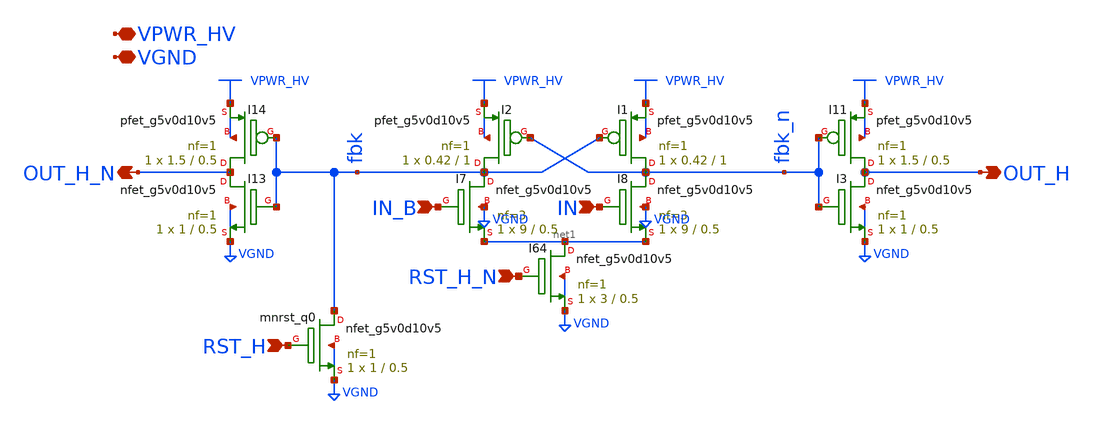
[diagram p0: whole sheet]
** sch_path: gpiov2_amux_ctl_lshv2hv.sch
* Copyright 2023 David Mitchell Bailey
* Licensed under the Apache License, Version 2.0 (the "License");
* you may not use this file except in compliance with the License.
* You may obtain a copy of the License at
* https://www.apache.org/licenses/LICENSE-2.0
* Unless required by applicable law or agreed to in writing, software
* distributed under the License is distributed on an "AS IS" BASIS,
* WITHOUT WARRANTIES OR CONDITIONS OF ANY KIND, either express or implied.
* See the License for the specific language governing permissions and
* limitations under the License.
**.subckt gpiov2_amux_ctl_lshv2hv RST_H OUT_H VPWR_HV VGND OUT_H_N RST_H_N IN_B IN
*.ipin RST_H
*.opin OUT_H
*.iopin VPWR_HV
*.iopin VGND
*.opin OUT_H_N
*.ipin RST_H_N
*.ipin IN_B
*.ipin IN
XI13 OUT_H_N fbk VGND VGND sky130_fd_pr__nfet_g5v0d10v5 L=0.5 W=1 nf=1 ad='int((nf+1)/2) * W/nf * 0.29'
+ as='int((nf+2)/2) * W/nf * 0.29' pd='2*int((nf+1)/2) * (W/nf + 0.29)' ps='2*int((nf+2)/2) * (W/nf + 0.29)'
+ nrd='0.29 / W' nrs='0.29 / W' sa=0 sb=0 sd=0 mult=1 m=1
XI14 OUT_H_N fbk VPWR_HV VPWR_HV sky130_fd_pr__pfet_g5v0d10v5 L=0.5 W=1.5 nf=1 ad='int((nf+1)/2) * W/nf * 0.29'
+ as='int((nf+2)/2) * W/nf * 0.29' pd='2*int((nf+1)/2) * (W/nf + 0.29)' ps='2*int((nf+2)/2) * (W/nf + 0.29)'
+ nrd='0.29 / W' nrs='0.29 / W' sa=0 sb=0 sd=0 mult=1 m=1
XI3 OUT_H fbk_n VGND VGND sky130_fd_pr__nfet_g5v0d10v5 L=0.5 W=1 nf=1 ad='int((nf+1)/2) * W/nf * 0.29'
+ as='int((nf+2)/2) * W/nf * 0.29' pd='2*int((nf+1)/2) * (W/nf + 0.29)' ps='2*int((nf+2)/2) * (W/nf + 0.29)'
+ nrd='0.29 / W' nrs='0.29 / W' sa=0 sb=0 sd=0 mult=1 m=1
XI11 OUT_H fbk_n VPWR_HV VPWR_HV sky130_fd_pr__pfet_g5v0d10v5 L=0.5 W=1.5 nf=1 ad='int((nf+1)/2) * W/nf * 0.29'
+ as='int((nf+2)/2) * W/nf * 0.29' pd='2*int((nf+1)/2) * (W/nf + 0.29)' ps='2*int((nf+2)/2) * (W/nf + 0.29)'
+ nrd='0.29 / W' nrs='0.29 / W' sa=0 sb=0 sd=0 mult=1 m=1
XI8 fbk_n IN net1 VGND sky130_fd_pr__nfet_g5v0d10v5 L=0.5 W=9 nf=3 ad='int((nf+1)/2) * W/nf * 0.29' as='int((nf+2)/2) * W/nf * 0.29'
+ pd='2*int((nf+1)/2) * (W/nf + 0.29)' ps='2*int((nf+2)/2) * (W/nf + 0.29)' nrd='0.29 / W' nrs='0.29 / W'
+ sa=0 sb=0 sd=0 mult=1 m=1
XI1 fbk_n fbk VPWR_HV VPWR_HV sky130_fd_pr__pfet_g5v0d10v5 L=1 W=0.42 nf=1 ad='int((nf+1)/2) * W/nf * 0.29'
+ as='int((nf+2)/2) * W/nf * 0.29' pd='2*int((nf+1)/2) * (W/nf + 0.29)' ps='2*int((nf+2)/2) * (W/nf + 0.29)'
+ nrd='0.29 / W' nrs='0.29 / W' sa=0 sb=0 sd=0 mult=1 m=1
XI7 fbk IN_B net1 VGND sky130_fd_pr__nfet_g5v0d10v5 L=0.5 W=9 nf=3 ad='int((nf+1)/2) * W/nf * 0.29' as='int((nf+2)/2) * W/nf * 0.29'
+ pd='2*int((nf+1)/2) * (W/nf + 0.29)' ps='2*int((nf+2)/2) * (W/nf + 0.29)' nrd='0.29 / W' nrs='0.29 / W'
+ sa=0 sb=0 sd=0 mult=1 m=1
XI2 fbk fbk_n VPWR_HV VPWR_HV sky130_fd_pr__pfet_g5v0d10v5 L=1 W=0.42 nf=1 ad='int((nf+1)/2) * W/nf * 0.29'
+ as='int((nf+2)/2) * W/nf * 0.29' pd='2*int((nf+1)/2) * (W/nf + 0.29)' ps='2*int((nf+2)/2) * (W/nf + 0.29)'
+ nrd='0.29 / W' nrs='0.29 / W' sa=0 sb=0 sd=0 mult=1 m=1
Xmnrst_q0 fbk RST_H VGND VGND sky130_fd_pr__nfet_g5v0d10v5 L=0.5 W=1 nf=1 ad='int((nf+1)/2) * W/nf * 0.29'
+ as='int((nf+2)/2) * W/nf * 0.29' pd='2*int((nf+1)/2) * (W/nf + 0.29)' ps='2*int((nf+2)/2) * (W/nf + 0.29)'
+ nrd='0.29 / W' nrs='0.29 / W' sa=0 sb=0 sd=0 mult=1 m=1
XI64 net1 RST_H_N VGND VGND sky130_fd_pr__nfet_g5v0d10v5 L=0.5 W=3 nf=1 ad='int((nf+1)/2) * W/nf * 0.29'
+ as='int((nf+2)/2) * W/nf * 0.29' pd='2*int((nf+1)/2) * (W/nf + 0.29)' ps='2*int((nf+2)/2) * (W/nf + 0.29)'
+ nrd='0.29 / W' nrs='0.29 / W' sa=0 sb=0 sd=0 mult=1 m=1
**.ends
.end
